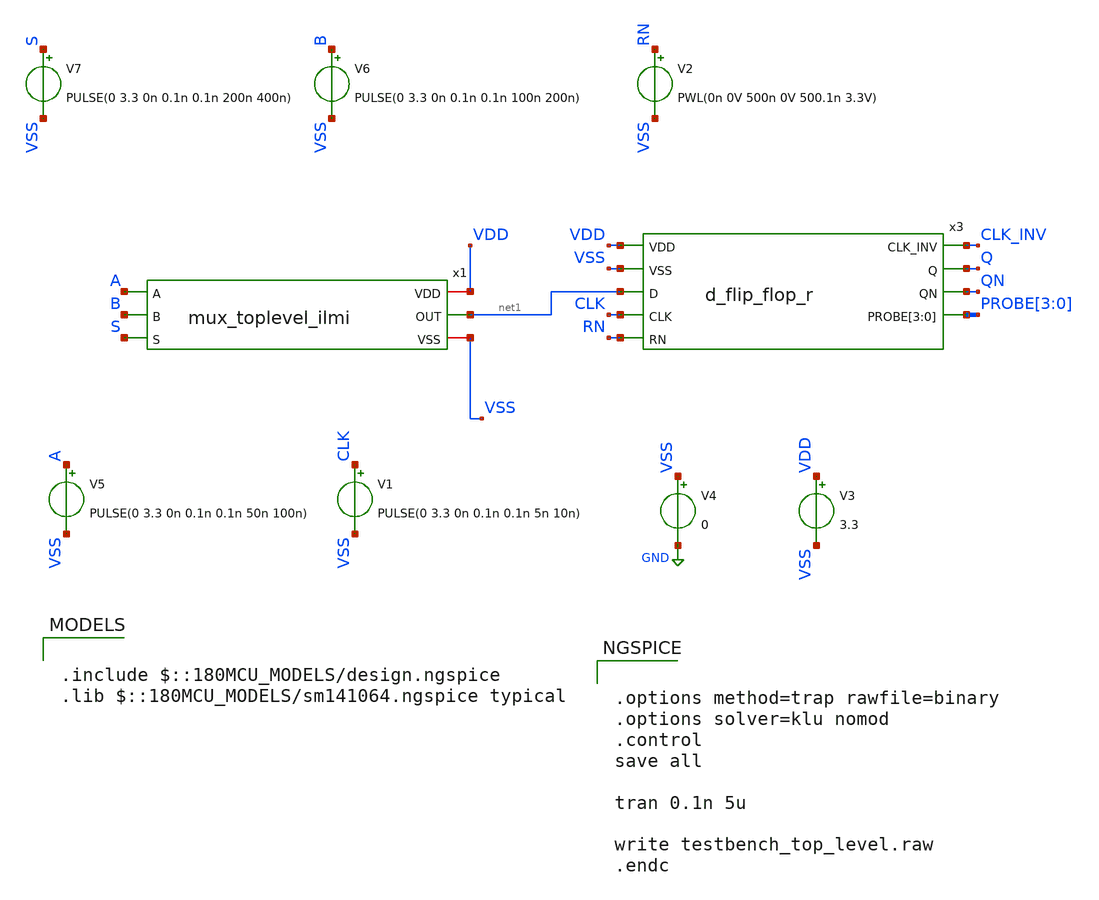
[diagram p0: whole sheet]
** sch_path: designs/schematics/testbench_top_level_mux_tg.sch
**.subckt testbench_top_level_mux_tg
V1 CLK VSS PULSE(0 3.3 0n 0.1n 0.1n 5n 10n)
V3 VDD VSS 3.3
V4 VSS GND 0
V5 A VSS PULSE(0 3.3 0n 0.1n 0.1n 50n 100n)
V6 B VSS PULSE(0 3.3 0n 0.1n 0.1n 100n 200n)
V7 S VSS PULSE(0 3.3 0n 0.1n 0.1n 200n 400n)
V2 RN VSS PWL(0n 0V 500n 0V 500.1n 3.3V)
x3 VDD CLK_INV VSS Q net1 QN CLK PROBE[3] PROBE[2] PROBE[1] PROBE[0] RN d_flip_flop_r
x1 VDD A net1 B VSS S mux_toplevel_ilmi
**** begin user architecture code

.include $::180MCU_MODELS/design.ngspice
.lib $::180MCU_MODELS/sm141064.ngspice typical



.options method=trap rawfile=binary
.options solver=klu nomod
.control
save all

tran 0.1n 5u

write testbench_top_level.raw
.endc


**** end user architecture code
**.ends
.GLOBAL GND
.end
